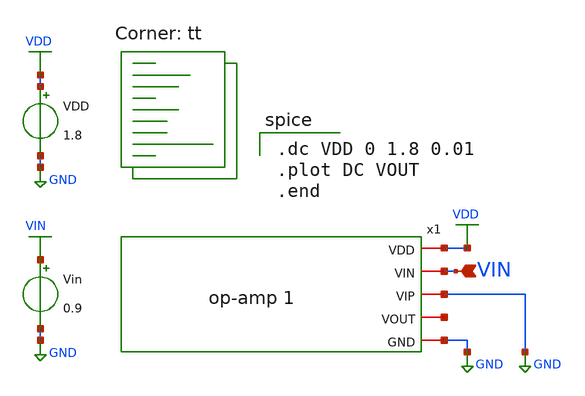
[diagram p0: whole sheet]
** sch_path: op-amp 1_tb.sch
**.subckt op-amp 1_tb VIN
*.ipin VIN
x1 VDD VIN GND net1 GND op-amp 1
VDD VDD GND 1.8
Vin VIN GND 0.9
**** begin user architecture code
.lib $::SKYWATER_MODELS/sky130.lib.spice tt

.dc VDD 0 1.8 0.01
.plot DC VOUT
.end

**** end user architecture code
**.ends

* expanding   symbol:  /home/kandiasrw/xschem/project/op-amp 1.sym # of pins=5
** sym_path: op-amp 1.sym
** sch_path: op-amp 1.sch
.subckt op-amp 1 VDD VIN VIP VOUT GND
*.iopin VDD
*.iopin GND
*.iopin VIN
*.iopin VOUT
*.iopin VIP
XM1 net2 net1 net6 GND sky130_fd_pr__nfet_01v8 L=0.15 W=1 nf=1 ad='int((nf+1)/2) * W/nf * 0.29' as='int((nf+2)/2) * W/nf * 0.29'
+ pd='2*int((nf+1)/2) * (W/nf + 0.29)' ps='2*int((nf+2)/2) * (W/nf + 0.29)' nrd='0.29 / W' nrs='0.29 / W'
+ sa=0 sb=0 sd=0 mult=1 m=1
XM2 net1 net1 GND GND sky130_fd_pr__nfet_01v8 L=0.15 W=1 nf=1 ad='int((nf+1)/2) * W/nf * 0.29' as='int((nf+2)/2) * W/nf * 0.29'
+ pd='2*int((nf+1)/2) * (W/nf + 0.29)' ps='2*int((nf+2)/2) * (W/nf + 0.29)' nrd='0.29 / W' nrs='0.29 / W'
+ sa=0 sb=0 sd=0 mult=1 m=1
XM3 net2 net2 VDD VDD sky130_fd_pr__pfet_01v8 L=0.15 W=1 nf=1 ad='int((nf+1)/2) * W/nf * 0.29' as='int((nf+2)/2) * W/nf * 0.29'
+ pd='2*int((nf+1)/2) * (W/nf + 0.29)' ps='2*int((nf+2)/2) * (W/nf + 0.29)' nrd='0.29 / W' nrs='0.29 / W'
+ sa=0 sb=0 sd=0 mult=1 m=1
XM4 net1 net2 VDD VDD sky130_fd_pr__pfet_01v8 L=0.15 W=1 nf=1 ad='int((nf+1)/2) * W/nf * 0.29' as='int((nf+2)/2) * W/nf * 0.29'
+ pd='2*int((nf+1)/2) * (W/nf + 0.29)' ps='2*int((nf+2)/2) * (W/nf + 0.29)' nrd='0.29 / W' nrs='0.29 / W'
+ sa=0 sb=0 sd=0 mult=1 m=1
XM5 net3 net3 VDD VDD sky130_fd_pr__pfet_01v8 L=0.15 W=1 nf=1 ad='int((nf+1)/2) * W/nf * 0.29' as='int((nf+2)/2) * W/nf * 0.29'
+ pd='2*int((nf+1)/2) * (W/nf + 0.29)' ps='2*int((nf+2)/2) * (W/nf + 0.29)' nrd='0.29 / W' nrs='0.29 / W'
+ sa=0 sb=0 sd=0 mult=1 m=1
XM6 net5 net3 VDD VDD sky130_fd_pr__pfet_01v8 L=0.15 W=1 nf=1 ad='int((nf+1)/2) * W/nf * 0.29' as='int((nf+2)/2) * W/nf * 0.29'
+ pd='2*int((nf+1)/2) * (W/nf + 0.29)' ps='2*int((nf+2)/2) * (W/nf + 0.29)' nrd='0.29 / W' nrs='0.29 / W'
+ sa=0 sb=0 sd=0 mult=1 m=1
XM7 net3 VIN net4 GND sky130_fd_pr__nfet_01v8 L=0.15 W=1 nf=1 ad='int((nf+1)/2) * W/nf * 0.29' as='int((nf+2)/2) * W/nf * 0.29'
+ pd='2*int((nf+1)/2) * (W/nf + 0.29)' ps='2*int((nf+2)/2) * (W/nf + 0.29)' nrd='0.29 / W' nrs='0.29 / W'
+ sa=0 sb=0 sd=0 mult=1 m=1
XM8 net5 VIP net4 GND sky130_fd_pr__nfet_01v8 L=0.15 W=1 nf=1 ad='int((nf+1)/2) * W/nf * 0.29' as='int((nf+2)/2) * W/nf * 0.29'
+ pd='2*int((nf+1)/2) * (W/nf + 0.29)' ps='2*int((nf+2)/2) * (W/nf + 0.29)' nrd='0.29 / W' nrs='0.29 / W'
+ sa=0 sb=0 sd=0 mult=1 m=1
XM9 net4 net1 GND GND sky130_fd_pr__nfet_01v8 L=0.15 W=1 nf=1 ad='int((nf+1)/2) * W/nf * 0.29' as='int((nf+2)/2) * W/nf * 0.29'
+ pd='2*int((nf+1)/2) * (W/nf + 0.29)' ps='2*int((nf+2)/2) * (W/nf + 0.29)' nrd='0.29 / W' nrs='0.29 / W'
+ sa=0 sb=0 sd=0 mult=1 m=1
XM10 VOUT net5 VDD VDD sky130_fd_pr__pfet_01v8 L=0.15 W=1 nf=1 ad='int((nf+1)/2) * W/nf * 0.29' as='int((nf+2)/2) * W/nf * 0.29'
+ pd='2*int((nf+1)/2) * (W/nf + 0.29)' ps='2*int((nf+2)/2) * (W/nf + 0.29)' nrd='0.29 / W' nrs='0.29 / W'
+ sa=0 sb=0 sd=0 mult=1 m=1
XM11 VOUT net1 GND GND sky130_fd_pr__nfet_01v8 L=0.15 W=1 nf=1 ad='int((nf+1)/2) * W/nf * 0.29' as='int((nf+2)/2) * W/nf * 0.29'
+ pd='2*int((nf+1)/2) * (W/nf + 0.29)' ps='2*int((nf+2)/2) * (W/nf + 0.29)' nrd='0.29 / W' nrs='0.29 / W'
+ sa=0 sb=0 sd=0 mult=1 m=1
XR3 GND net6 net8 sky130_fd_pr__res_high_po_0p35 L=1.5 mult=2 m=2
XR4 net7 net5 net9 sky130_fd_pr__res_high_po_0p35 L=0.35 mult=1 m=1
XC3 VOUT GND sky130_fd_pr__cap_mim_m3_1 W=1 L=1 MF=1 m=1
XC1 VOUT net7 sky130_fd_pr__cap_mim_m3_1 W=1 L=1 MF=1 m=1
.ends

.GLOBAL VDD
.GLOBAL GND
.GLOBAL VIN
.end
